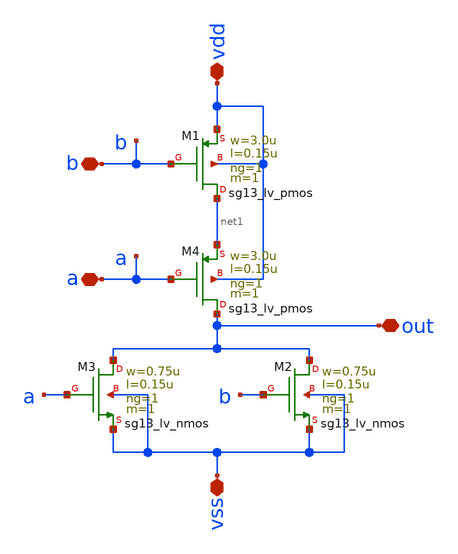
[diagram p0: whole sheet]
** sch_path: design/blocks/norgate/schematic/nor.sch
**.subckt nor vdd b vss out a
*.iopin vdd
*.iopin b
*.iopin vss
*.iopin out
*.iopin a
XM1 net1 b vdd vdd sg13_lv_pmos w=3.0u l=0.15u ng=1 m=1 mm_ok=1
XM2 out b vss vss sg13_lv_nmos w=0.75u l=0.15u ng=1 m=1 mm_ok=1
XM3 out a vss vss sg13_lv_nmos w=0.75u l=0.15u ng=1 m=1 mm_ok=1
XM4 out a net1 vdd sg13_lv_pmos w=3.0u l=0.15u ng=1 m=1 mm_ok=1
**.ends
.end
